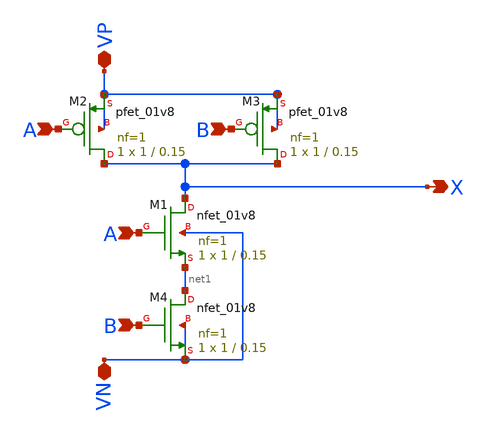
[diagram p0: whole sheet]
** sch_path: projekat_spice/layout/nand/NAND.sch
**.subckt NAND A A B B VP VN X
*.ipin A
*.ipin A
*.ipin B
*.ipin B
*.iopin VP
*.iopin VN
*.opin X
XM1 X A net1 VN sky130_fd_pr__nfet_01v8 L=0.15 W=1 nf=1 ad='int((nf+1)/2) * W/nf * 0.29' as='int((nf+2)/2) * W/nf * 0.29'
+ pd='2*int((nf+1)/2) * (W/nf + 0.29)' ps='2*int((nf+2)/2) * (W/nf + 0.29)' nrd='0.29 / W' nrs='0.29 / W'
+ sa=0 sb=0 sd=0 mult=1 m=1
XM2 X A VP VP sky130_fd_pr__pfet_01v8 L=0.15 W=1 nf=1 ad='int((nf+1)/2) * W/nf * 0.29' as='int((nf+2)/2) * W/nf * 0.29'
+ pd='2*int((nf+1)/2) * (W/nf + 0.29)' ps='2*int((nf+2)/2) * (W/nf + 0.29)' nrd='0.29 / W' nrs='0.29 / W'
+ sa=0 sb=0 sd=0 mult=1 m=1
XM3 X B VP VP sky130_fd_pr__pfet_01v8 L=0.15 W=1 nf=1 ad='int((nf+1)/2) * W/nf * 0.29' as='int((nf+2)/2) * W/nf * 0.29'
+ pd='2*int((nf+1)/2) * (W/nf + 0.29)' ps='2*int((nf+2)/2) * (W/nf + 0.29)' nrd='0.29 / W' nrs='0.29 / W'
+ sa=0 sb=0 sd=0 mult=1 m=1
XM4 net1 B VN VN sky130_fd_pr__nfet_01v8 L=0.15 W=1 nf=1 ad='int((nf+1)/2) * W/nf * 0.29' as='int((nf+2)/2) * W/nf * 0.29'
+ pd='2*int((nf+1)/2) * (W/nf + 0.29)' ps='2*int((nf+2)/2) * (W/nf + 0.29)' nrd='0.29 / W' nrs='0.29 / W'
+ sa=0 sb=0 sd=0 mult=1 m=1
**.ends
.end
